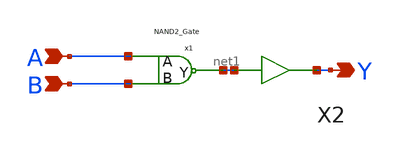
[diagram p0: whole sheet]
** sch_path: gates/AND2.sch
**.subckt AND2 Y A B
*.opin Y
*.ipin A
*.ipin B
x1 A net1 B NAND2_Gate
X2 net1 Y inv_vtc
**.ends

* expanding   symbol:  NAND2_Gate.sym # of pins=3
** sym_path: gates/NAND2_Gate.sym
** sch_path: gates/NAND2_Gate.sch
.subckt NAND2_Gate A Y B
*.ipin A
*.ipin B
*.opin Y
XM1 Y A net1 GND sky130_fd_pr__nfet_01v8 L=0.15 W=1 nf=1 ad='int((nf+1)/2) * W/nf * 0.29' as='int((nf+2)/2) * W/nf * 0.29'
+ pd='2*int((nf+1)/2) * (W/nf + 0.29)' ps='2*int((nf+2)/2) * (W/nf + 0.29)' nrd='0.29 / W' nrs='0.29 / W'
+ sa=0 sb=0 sd=0 mult=1 m=1
XM2 net1 B GND GND sky130_fd_pr__nfet_01v8 L=0.15 W=1 nf=1 ad='int((nf+1)/2) * W/nf * 0.29' as='int((nf+2)/2) * W/nf * 0.29'
+ pd='2*int((nf+1)/2) * (W/nf + 0.29)' ps='2*int((nf+2)/2) * (W/nf + 0.29)' nrd='0.29 / W' nrs='0.29 / W'
+ sa=0 sb=0 sd=0 mult=1 m=1
XM3 Y A VDD VDD sky130_fd_pr__pfet_01v8 L=0.15 W=1 nf=1 ad='int((nf+1)/2) * W/nf * 0.29' as='int((nf+2)/2) * W/nf * 0.29'
+ pd='2*int((nf+1)/2) * (W/nf + 0.29)' ps='2*int((nf+2)/2) * (W/nf + 0.29)' nrd='0.29 / W' nrs='0.29 / W'
+ sa=0 sb=0 sd=0 mult=1 m=1
XM4 Y B VDD VDD sky130_fd_pr__pfet_01v8 L=0.15 W=1 nf=1 ad='int((nf+1)/2) * W/nf * 0.29' as='int((nf+2)/2) * W/nf * 0.29'
+ pd='2*int((nf+1)/2) * (W/nf + 0.29)' ps='2*int((nf+2)/2) * (W/nf + 0.29)' nrd='0.29 / W' nrs='0.29 / W'
+ sa=0 sb=0 sd=0 mult=1 m=1
.ends


* expanding   symbol:  /home/apn/test_xschem_sky130/inv_vtc.sym # of pins=2
** sym_path: gates/inv_vtc.sym
** sch_path: gates/inv_vtc.sch
.subckt inv_vtc A Y
*.ipin A
*.opin Y
XM1 Y A VDD VDD sky130_fd_pr__pfet_01v8 L=0.15 W=2 nf=1 ad='int((nf+1)/2) * W/nf * 0.29' as='int((nf+2)/2) * W/nf * 0.29'
+ pd='2*int((nf+1)/2) * (W/nf + 0.29)' ps='2*int((nf+2)/2) * (W/nf + 0.29)' nrd='0.29 / W' nrs='0.29 / W'
+ sa=0 sb=0 sd=0 mult=1 m=1
XM2 Y A GND GND sky130_fd_pr__nfet_01v8 L=0.15 W=1 nf=1 ad='int((nf+1)/2) * W/nf * 0.29' as='int((nf+2)/2) * W/nf * 0.29'
+ pd='2*int((nf+1)/2) * (W/nf + 0.29)' ps='2*int((nf+2)/2) * (W/nf + 0.29)' nrd='0.29 / W' nrs='0.29 / W'
+ sa=0 sb=0 sd=0 mult=1 m=1
.ends

.GLOBAL VDD
.GLOBAL GND
.end
